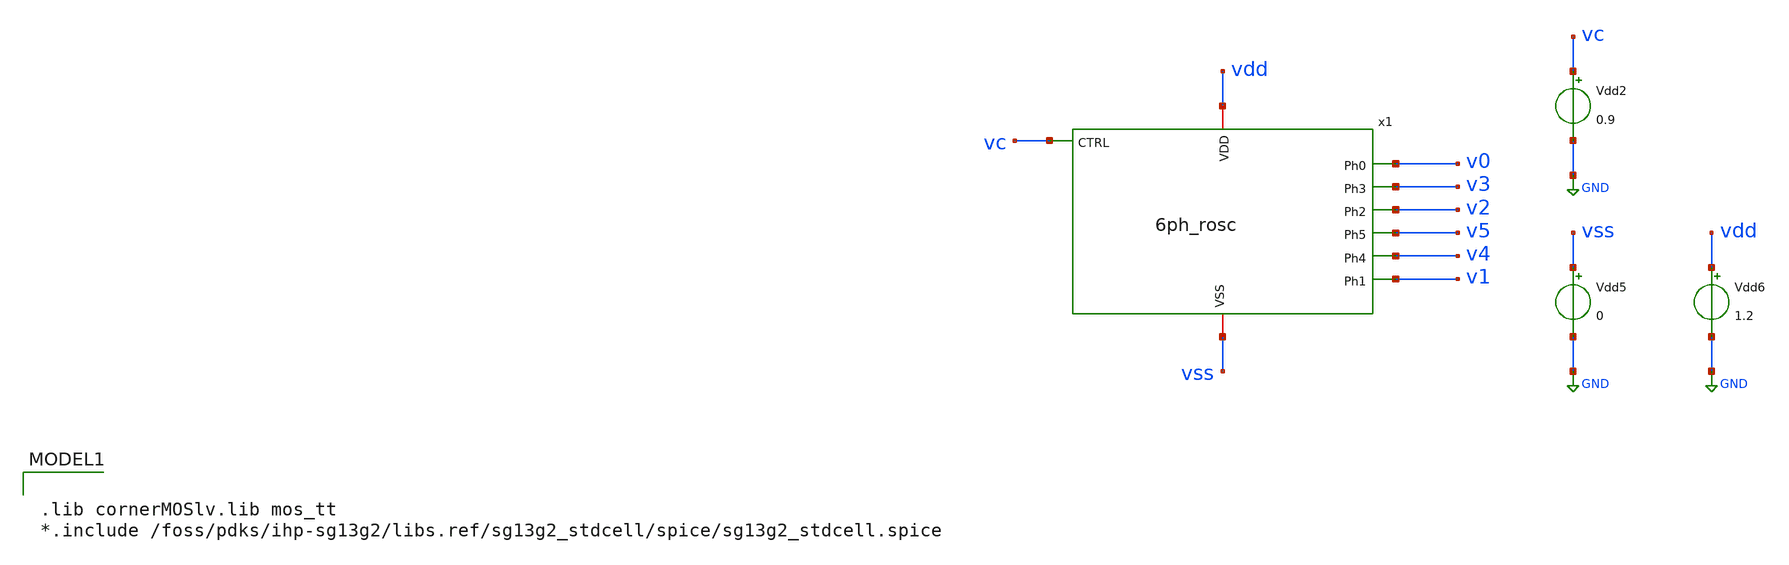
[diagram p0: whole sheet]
** sch_path: verification/testbenches/tb_6ph_rosc.sch
**.subckt tb_6ph_rosc
x1 vc v0 v3 v2 v5 v4 v1 vss vdd 6ph_rosc
Vdd2 vc GND 0.9
Vdd5 vss GND 0
Vdd6 vdd GND 1.2
**** begin user architecture code

.lib cornerMOSlv.lib mos_tt
*.include /foss/pdks/ihp-sg13g2/libs.ref/sg13g2_stdcell/spice/sg13g2_stdcell.spice




.options rshunt = 1e12
.save v(v0) v(v1) v(v2) v(v3) v(v4) v(v5) v(v6) v(v0_pex) v(v1_pex) v(v2_pex) v(v3_pex) v(v4_pex) v(v5_pex) v(v6_pex)
.tran 2p 20n


.control
run
set color0=white

set filetype = ascii
write 6ph_rosc.raw

*let period_0 = T0
*let period_1 = T1
*let period_2 = T2


meas tran T0 TRIG v(v0) VAL=0.6 RISE=5 TARG v(v0) VAL=0.6 RISE=6
meas tran T0_pex TRIG v(v0_pex) VAL=0.6 RISE=5 TARG v(v0_pex) VAL=0.6 RISE=6

let freq_0 = 1/T0

plot freq_0

.endc


**** end user architecture code
**.ends
.GLOBAL GND
.end
